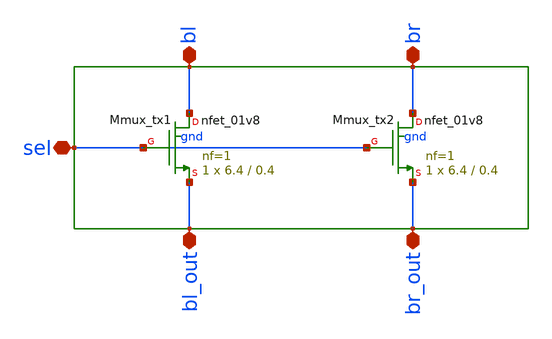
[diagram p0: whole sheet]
** sch_path: sram_2_64_scn4m_lcc/column_mux.sch
**.subckt column_mux bl br sel bl_out br_out
*.iopin bl
*.iopin br
*.iopin sel
*.iopin bl_out
*.iopin br_out
XMmux_tx1 bl sel bl_out gnd sky130_fd_pr__nfet_01v8 L=0.4 W=6.4 nf=1 ad='int((nf+1)/2) * W/nf * 0.29'
+ as='int((nf+2)/2) * W/nf * 0.29' pd='2*int((nf+1)/2) * (W/nf + 0.29)' ps='2*int((nf+2)/2) * (W/nf + 0.29)'
+ nrd='0.29 / W' nrs='0.29 / W' sa=0 sb=0 sd=0 mult=1 m=1
XMmux_tx2 br sel br_out gnd sky130_fd_pr__nfet_01v8 L=0.4 W=6.4 nf=1 ad='int((nf+1)/2) * W/nf * 0.29'
+ as='int((nf+2)/2) * W/nf * 0.29' pd='2*int((nf+1)/2) * (W/nf + 0.29)' ps='2*int((nf+2)/2) * (W/nf + 0.29)'
+ nrd='0.29 / W' nrs='0.29 / W' sa=0 sb=0 sd=0 mult=1 m=1
**.ends
.end
